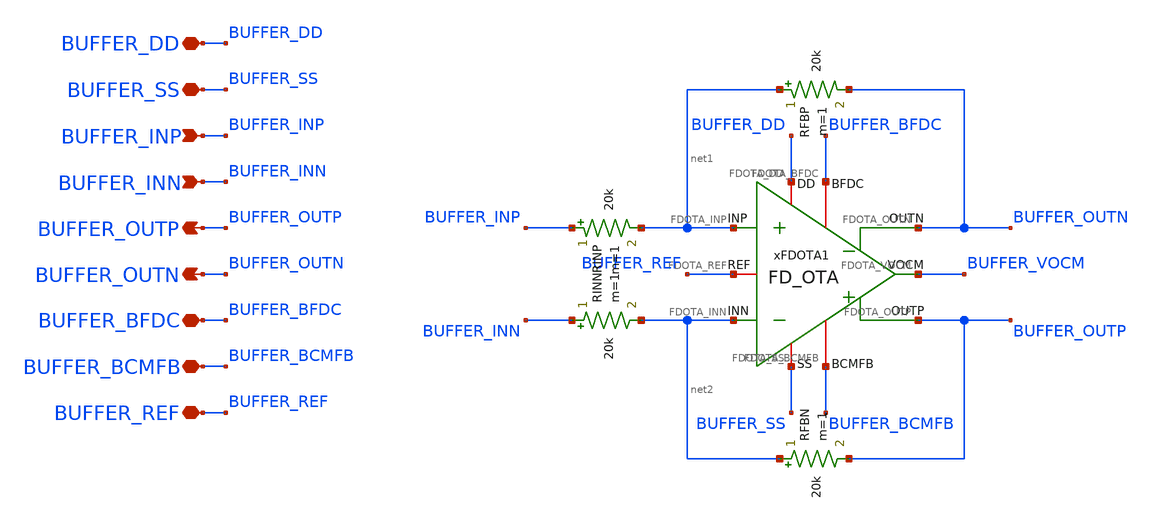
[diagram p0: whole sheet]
** sch_path: Design_Files/IC Design/Schematic/AFE_BLOCKS/BUFFER/BUFFER.sch
**.subckt BUFFER BUFFER_DD BUFFER_SS BUFFER_INP BUFFER_INN BUFFER_OUTP BUFFER_BFDC BUFFER_OUTN
*+ BUFFER_BCMFB BUFFER_REF
*.iopin BUFFER_DD
*.iopin BUFFER_SS
*.ipin BUFFER_INP
*.ipin BUFFER_INN
*.opin BUFFER_OUTP
*.iopin BUFFER_BFDC
*.opin BUFFER_OUTN
*.iopin BUFFER_BCMFB
*.iopin BUFFER_REF
RFBP net1 BUFFER_OUTN 20k m=1
xFDOTA1 BUFFER_DD BUFFER_SS net1 net2 BUFFER_OUTN BUFFER_BFDC BUFFER_OUTP BUFFER_BCMFB BUFFER_REF
+ BUFFER_VOCM FD_OTA
RINN BUFFER_INN net2 20k m=1
RINP BUFFER_INP net1 20k m=1
RFBN net2 BUFFER_OUTP 20k m=1
**.ends
.end
